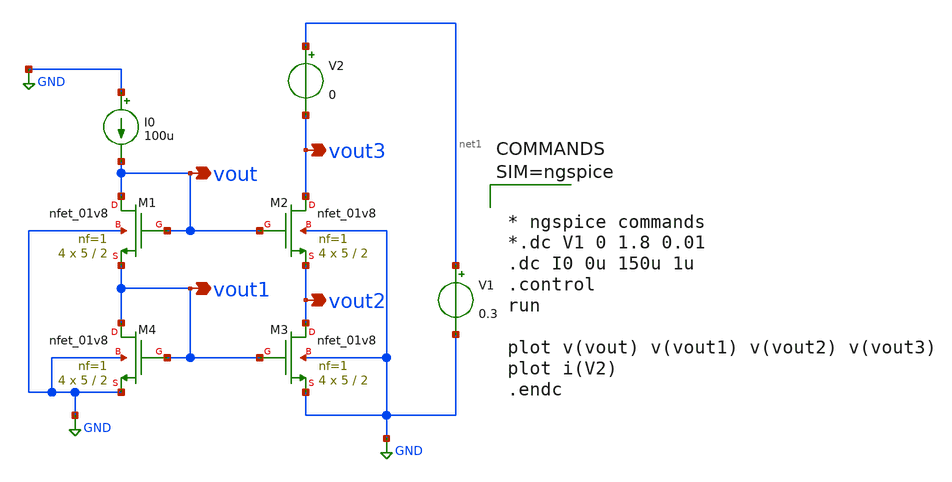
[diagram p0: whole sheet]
** sch_path: xschem/cascade_nmos.sch
**.subckt cascade_nmos vout vout1 vout3 vout2
*.opin vout
*.opin vout1
*.opin vout3
*.opin vout2
XM2 vout3 vout vout2 GND sky130_fd_pr__nfet_01v8 L=2 W=5 nf=1 ad='int((1 + 1)/2) * 5 / 1 * 0.29' as='int((1 + 2)/2) * 5 / 1 * 0.29'
+ pd='2*int((1 + 1)/2) * (5 / 1 + 0.29)' ps='2*int((1 + 2)/2) * (5 / 1 + 0.29)' nrd='0.29 / 5 ' nrs='0.29 / 5 '
+ sa=0 sb=0 sd=0 mult=4 m=4
XM1 vout vout vout1 GND sky130_fd_pr__nfet_01v8 L=2 W=5 nf=1 ad='int((1 + 1)/2) * 5 / 1 * 0.29' as='int((1 + 2)/2) * 5 / 1 * 0.29'
+ pd='2*int((1 + 1)/2) * (5 / 1 + 0.29)' ps='2*int((1 + 2)/2) * (5 / 1 + 0.29)' nrd='0.29 / 5 ' nrs='0.29 / 5 '
+ sa=0 sb=0 sd=0 mult=4 m=4
XM3 vout2 vout1 GND GND sky130_fd_pr__nfet_01v8 L=2 W=5 nf=1 ad='int((1 + 1)/2) * 5 / 1 * 0.29' as='int((1 + 2)/2) * 5 / 1 * 0.29'
+ pd='2*int((1 + 1)/2) * (5 / 1 + 0.29)' ps='2*int((1 + 2)/2) * (5 / 1 + 0.29)' nrd='0.29 / 5 ' nrs='0.29 / 5 '
+ sa=0 sb=0 sd=0 mult=4 m=4
XM4 vout1 vout1 GND GND sky130_fd_pr__nfet_01v8 L=2 W=5 nf=1 ad='int((1 + 1)/2) * 5 / 1 * 0.29' as='int((1 + 2)/2) * 5 / 1 * 0.29'
+ pd='2*int((1 + 1)/2) * (5 / 1 + 0.29)' ps='2*int((1 + 2)/2) * (5 / 1 + 0.29)' nrd='0.29 / 5 ' nrs='0.29 / 5 '
+ sa=0 sb=0 sd=0 mult=4 m=4
I0 GND vout 100u
V1 net1 GND 0.3
V2 net1 vout3 0
**** begin user architecture code

** opencircuitdesign pdks install
.lib $::SKYWATER_MODELS/sky130.lib.spice tt




* ngspice commands
*.dc V1 0 1.8 0.01
.dc I0 0u 150u 1u
.control
run

plot v(vout) v(vout1) v(vout2) v(vout3)
plot i(V2)
.endc



**** end user architecture code
**.ends
.GLOBAL GND
.end
